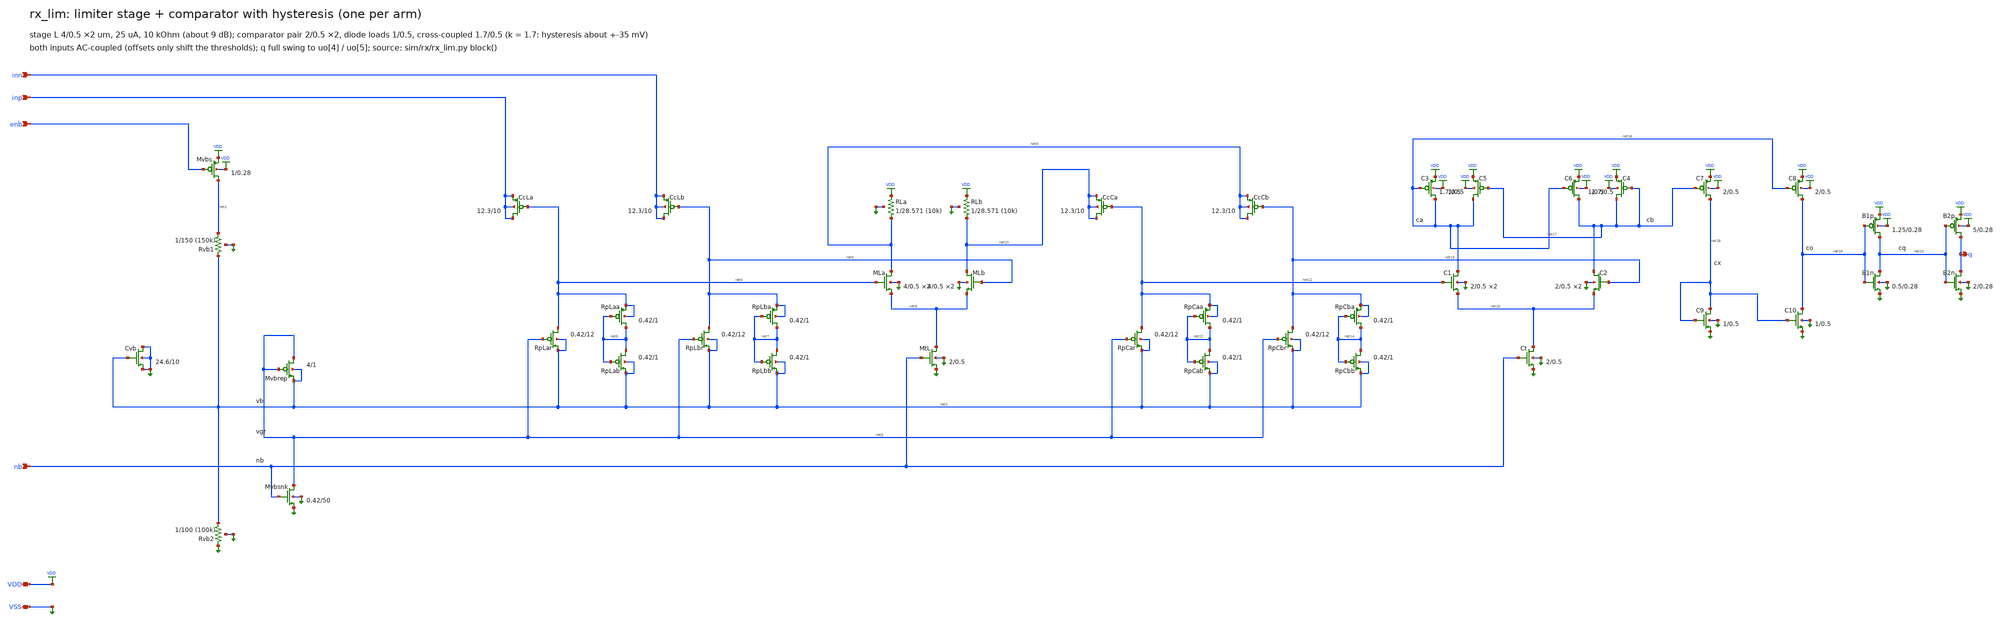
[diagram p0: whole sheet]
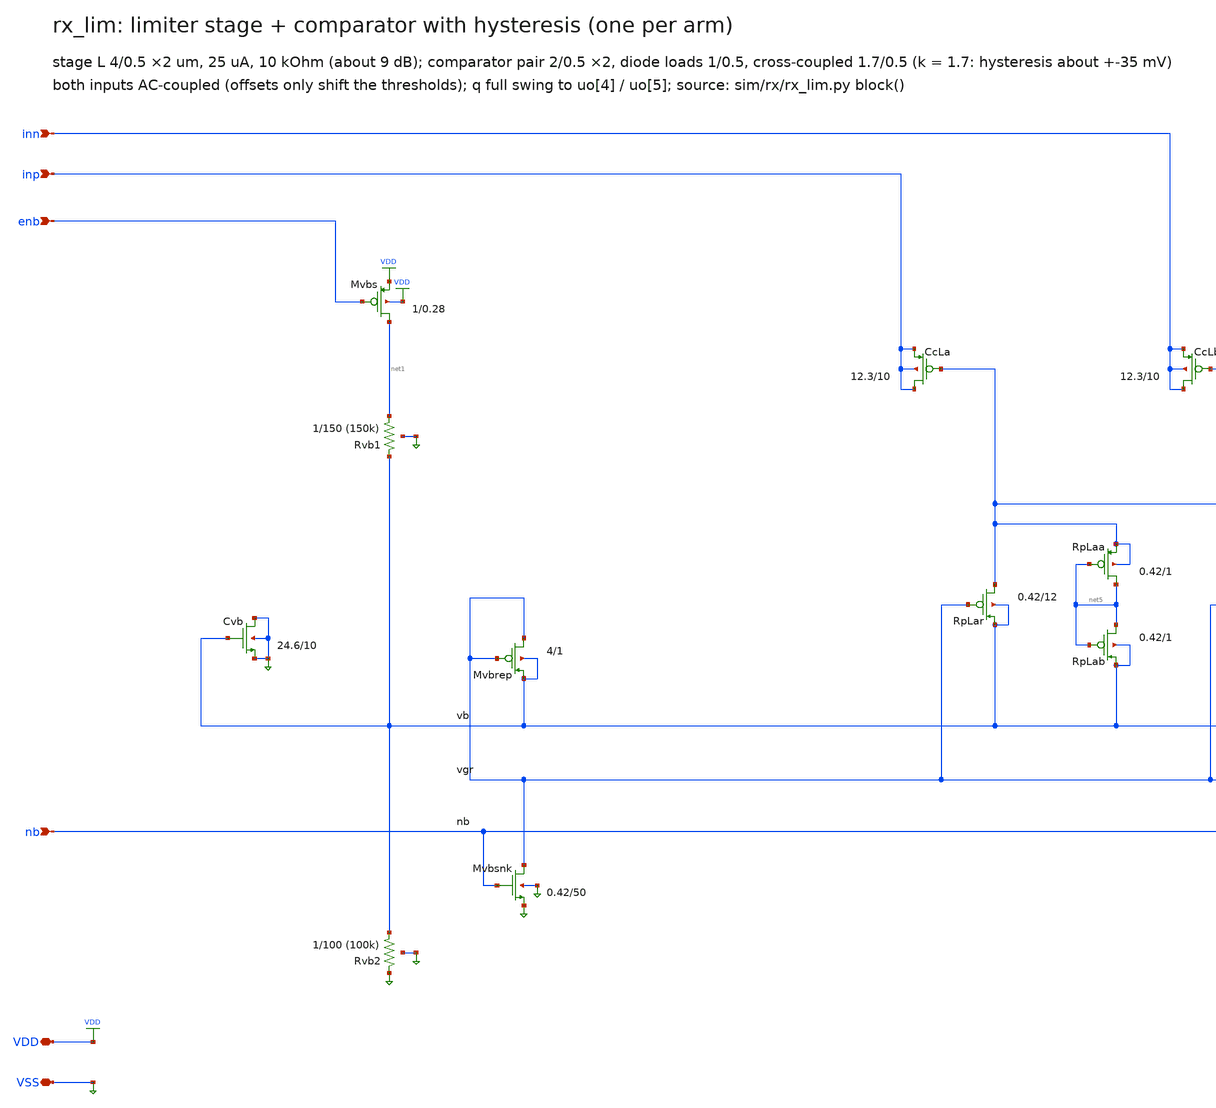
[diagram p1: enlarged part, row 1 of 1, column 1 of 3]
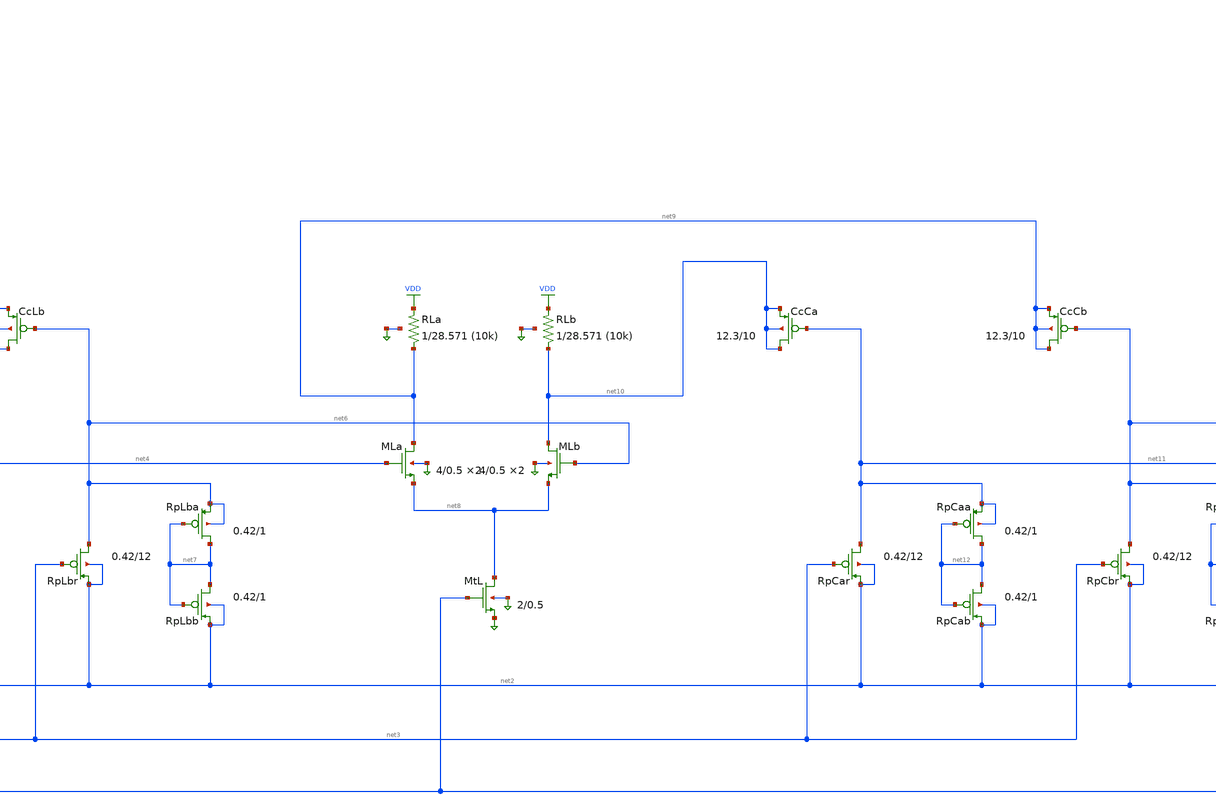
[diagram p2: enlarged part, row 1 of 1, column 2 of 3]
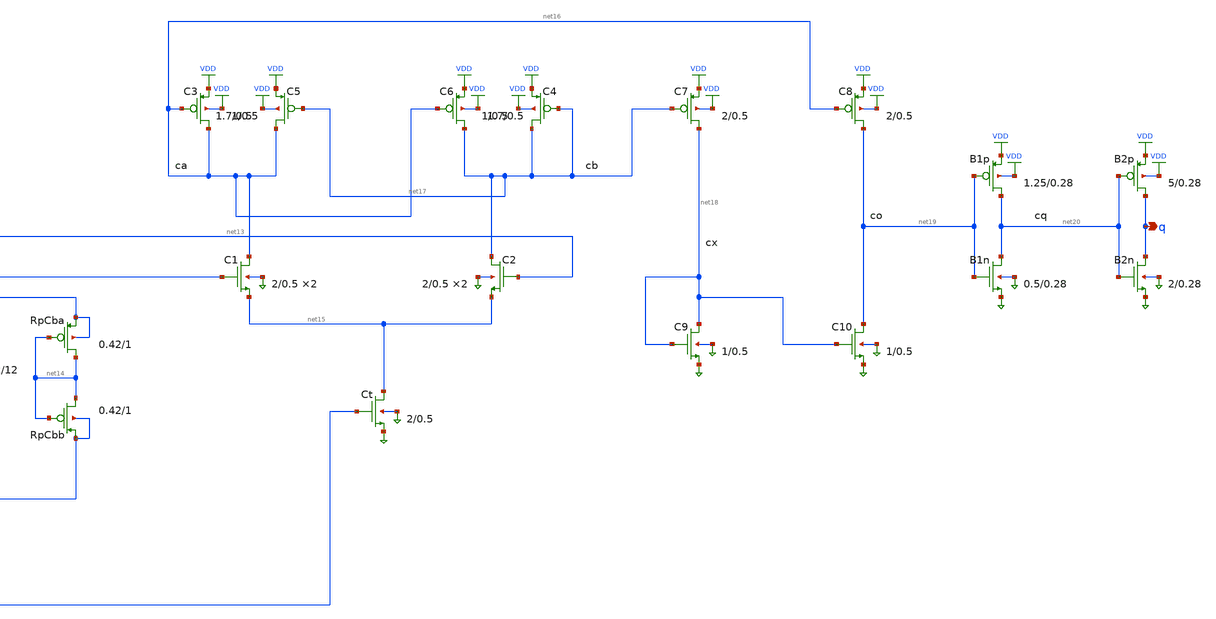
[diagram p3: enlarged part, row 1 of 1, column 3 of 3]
** sch_path: xschem/rx_lim.sch
**.subckt rx_lim VDD VSS inp inn q nb enb
*.iopin VDD
*.iopin VSS
*.ipin inp
*.ipin inn
*.opin q
*.ipin nb
*.ipin enb
XMvbs net1 enb VDD VDD pfet_03v3 L=0.28u W=1.0u nf=1 ad=0.5p as=0.5p pd=3.0u ps=3.0u nrd=0 nrs=0
+ sa=0 sb=0 sd=0 m=1
XRvb1 net1 net2 VSS ppolyf_u_1k r_width=1.0e-6 r_length=150.0e-6 m=1
XRvb2 net2 VSS VSS ppolyf_u_1k r_width=1.0e-6 r_length=100.0e-6 m=1
XCvb VSS net2 VSS VSS nfet_03v3 L=10.0u W=24.57u nf=1 ad=12.285p as=12.285p pd=50.14u ps=50.14u
+ nrd=0 nrs=0 sa=0 sb=0 sd=0 m=1
XMvbrep net3 net3 net2 net2 pfet_03v3 L=1.0u W=4.0u nf=1 ad=2.0p as=2.0p pd=9.0u ps=9.0u nrd=0 nrs=0
+ sa=0 sb=0 sd=0 m=1
XMvbsnk net3 nb VSS VSS nfet_03v3 L=49.99999999999999u W=0.41999999999999993u nf=1
+ ad=0.20999999999999996p as=0.20999999999999996p pd=1.8399999999999999u ps=1.8399999999999999u nrd=0 nrs=0 sa=0 sb=0 sd=0
+ m=1
XCcLa inp net4 inp inp pfet_03v3 L=10.0u W=12.285u nf=1 ad=6.1425p as=6.1425p pd=25.57u ps=25.57u
+ nrd=0 nrs=0 sa=0 sb=0 sd=0 m=1
XRpLar net4 net3 net2 net2 pfet_03v3 L=12.0u W=0.41999999999999993u nf=1 ad=0.20999999999999996p
+ as=0.20999999999999996p pd=1.8399999999999999u ps=1.8399999999999999u nrd=0 nrs=0 sa=0 sb=0 sd=0 m=1
XRpLaa net5 net5 net4 net4 pfet_03v3 L=1.0u W=0.41999999999999993u nf=1 ad=0.20999999999999996p
+ as=0.20999999999999996p pd=1.8399999999999999u ps=1.8399999999999999u nrd=0 nrs=0 sa=0 sb=0 sd=0 m=1
XRpLab net5 net5 net2 net2 pfet_03v3 L=1.0u W=0.41999999999999993u nf=1 ad=0.20999999999999996p
+ as=0.20999999999999996p pd=1.8399999999999999u ps=1.8399999999999999u nrd=0 nrs=0 sa=0 sb=0 sd=0 m=1
XCcLb inn net6 inn inn pfet_03v3 L=10.0u W=12.285u nf=1 ad=6.1425p as=6.1425p pd=25.57u ps=25.57u
+ nrd=0 nrs=0 sa=0 sb=0 sd=0 m=1
XRpLbr net6 net3 net2 net2 pfet_03v3 L=12.0u W=0.41999999999999993u nf=1 ad=0.20999999999999996p
+ as=0.20999999999999996p pd=1.8399999999999999u ps=1.8399999999999999u nrd=0 nrs=0 sa=0 sb=0 sd=0 m=1
XRpLba net7 net7 net6 net6 pfet_03v3 L=1.0u W=0.41999999999999993u nf=1 ad=0.20999999999999996p
+ as=0.20999999999999996p pd=1.8399999999999999u ps=1.8399999999999999u nrd=0 nrs=0 sa=0 sb=0 sd=0 m=1
XRpLbb net7 net7 net2 net2 pfet_03v3 L=1.0u W=0.41999999999999993u nf=1 ad=0.20999999999999996p
+ as=0.20999999999999996p pd=1.8399999999999999u ps=1.8399999999999999u nrd=0 nrs=0 sa=0 sb=0 sd=0 m=1
XMLa net9 net4 net8 VSS nfet_03v3 L=0.5u W=4.0u nf=1 ad=2.0p as=2.0p pd=9.0u ps=9.0u nrd=0 nrs=0
+ sa=0 sb=0 sd=0 m=2
XMLb net10 net6 net8 VSS nfet_03v3 L=0.5u W=4.0u nf=1 ad=2.0p as=2.0p pd=9.0u ps=9.0u nrd=0 nrs=0
+ sa=0 sb=0 sd=0 m=2
XMtL net8 nb VSS VSS nfet_03v3 L=0.5u W=2.0u nf=1 ad=1.0p as=1.0p pd=5.0u ps=5.0u nrd=0 nrs=0 sa=0
+ sb=0 sd=0 m=1
XRLa net9 VDD VSS ppolyf_u r_width=1.0e-6 r_length=28.571e-6 m=1
XRLb net10 VDD VSS ppolyf_u r_width=1.0e-6 r_length=28.571e-6 m=1
XCcCa net10 net11 net10 net10 pfet_03v3 L=10.0u W=12.285u nf=1 ad=6.1425p as=6.1425p pd=25.57u
+ ps=25.57u nrd=0 nrs=0 sa=0 sb=0 sd=0 m=1
XRpCar net11 net3 net2 net2 pfet_03v3 L=12.0u W=0.41999999999999993u nf=1 ad=0.20999999999999996p
+ as=0.20999999999999996p pd=1.8399999999999999u ps=1.8399999999999999u nrd=0 nrs=0 sa=0 sb=0 sd=0 m=1
XRpCaa net12 net12 net11 net11 pfet_03v3 L=1.0u W=0.41999999999999993u nf=1 ad=0.20999999999999996p
+ as=0.20999999999999996p pd=1.8399999999999999u ps=1.8399999999999999u nrd=0 nrs=0 sa=0 sb=0 sd=0 m=1
XRpCab net12 net12 net2 net2 pfet_03v3 L=1.0u W=0.41999999999999993u nf=1 ad=0.20999999999999996p
+ as=0.20999999999999996p pd=1.8399999999999999u ps=1.8399999999999999u nrd=0 nrs=0 sa=0 sb=0 sd=0 m=1
XCcCb net9 net13 net9 net9 pfet_03v3 L=10.0u W=12.285u nf=1 ad=6.1425p as=6.1425p pd=25.57u
+ ps=25.57u nrd=0 nrs=0 sa=0 sb=0 sd=0 m=1
XRpCbr net13 net3 net2 net2 pfet_03v3 L=12.0u W=0.41999999999999993u nf=1 ad=0.20999999999999996p
+ as=0.20999999999999996p pd=1.8399999999999999u ps=1.8399999999999999u nrd=0 nrs=0 sa=0 sb=0 sd=0 m=1
XRpCba net14 net14 net13 net13 pfet_03v3 L=1.0u W=0.41999999999999993u nf=1 ad=0.20999999999999996p
+ as=0.20999999999999996p pd=1.8399999999999999u ps=1.8399999999999999u nrd=0 nrs=0 sa=0 sb=0 sd=0 m=1
XRpCbb net14 net14 net2 net2 pfet_03v3 L=1.0u W=0.41999999999999993u nf=1 ad=0.20999999999999996p
+ as=0.20999999999999996p pd=1.8399999999999999u ps=1.8399999999999999u nrd=0 nrs=0 sa=0 sb=0 sd=0 m=1
XC1 net16 net11 net15 VSS nfet_03v3 L=0.5u W=2.0u nf=1 ad=1.0p as=1.0p pd=5.0u ps=5.0u nrd=0 nrs=0
+ sa=0 sb=0 sd=0 m=2
XC2 net17 net13 net15 VSS nfet_03v3 L=0.5u W=2.0u nf=1 ad=1.0p as=1.0p pd=5.0u ps=5.0u nrd=0 nrs=0
+ sa=0 sb=0 sd=0 m=2
XCt net15 nb VSS VSS nfet_03v3 L=0.5u W=2.0u nf=1 ad=1.0p as=1.0p pd=5.0u ps=5.0u nrd=0 nrs=0 sa=0
+ sb=0 sd=0 m=1
XC3 net16 net16 VDD VDD pfet_03v3 L=0.5u W=1.0u nf=1 ad=0.5p as=0.5p pd=3.0u ps=3.0u nrd=0 nrs=0
+ sa=0 sb=0 sd=0 m=1
XC5 net16 net17 VDD VDD pfet_03v3 L=0.5u W=1.6999999999999997u nf=1 ad=0.8499999999999999p
+ as=0.8499999999999999p pd=4.3999999999999995u ps=4.3999999999999995u nrd=0 nrs=0 sa=0 sb=0 sd=0 m=1
XC4 net17 net17 VDD VDD pfet_03v3 L=0.5u W=1.0u nf=1 ad=0.5p as=0.5p pd=3.0u ps=3.0u nrd=0 nrs=0
+ sa=0 sb=0 sd=0 m=1
XC6 net17 net16 VDD VDD pfet_03v3 L=0.5u W=1.6999999999999997u nf=1 ad=0.8499999999999999p
+ as=0.8499999999999999p pd=4.3999999999999995u ps=4.3999999999999995u nrd=0 nrs=0 sa=0 sb=0 sd=0 m=1
XC7 net18 net17 VDD VDD pfet_03v3 L=0.5u W=2.0u nf=1 ad=1.0p as=1.0p pd=5.0u ps=5.0u nrd=0 nrs=0
+ sa=0 sb=0 sd=0 m=1
XC8 net19 net16 VDD VDD pfet_03v3 L=0.5u W=2.0u nf=1 ad=1.0p as=1.0p pd=5.0u ps=5.0u nrd=0 nrs=0
+ sa=0 sb=0 sd=0 m=1
XC9 net18 net18 VSS VSS nfet_03v3 L=0.5u W=1.0u nf=1 ad=0.5p as=0.5p pd=3.0u ps=3.0u nrd=0 nrs=0
+ sa=0 sb=0 sd=0 m=1
XC10 net19 net18 VSS VSS nfet_03v3 L=0.5u W=1.0u nf=1 ad=0.5p as=0.5p pd=3.0u ps=3.0u nrd=0 nrs=0
+ sa=0 sb=0 sd=0 m=1
XB1p net20 net19 VDD VDD pfet_03v3 L=0.28u W=1.25u nf=1 ad=0.625p as=0.625p pd=3.5u ps=3.5u nrd=0
+ nrs=0 sa=0 sb=0 sd=0 m=1
XB1n net20 net19 VSS VSS nfet_03v3 L=0.28u W=0.5u nf=1 ad=0.25p as=0.25p pd=2.0u ps=2.0u nrd=0 nrs=0
+ sa=0 sb=0 sd=0 m=1
XB2p q net20 VDD VDD pfet_03v3 L=0.28u W=5.0u nf=1 ad=2.5p as=2.5p pd=11.0u ps=11.0u nrd=0 nrs=0
+ sa=0 sb=0 sd=0 m=1
XB2n q net20 VSS VSS nfet_03v3 L=0.28u W=2.0u nf=1 ad=1.0p as=1.0p pd=5.0u ps=5.0u nrd=0 nrs=0 sa=0
+ sb=0 sd=0 m=1
**.ends
.end
